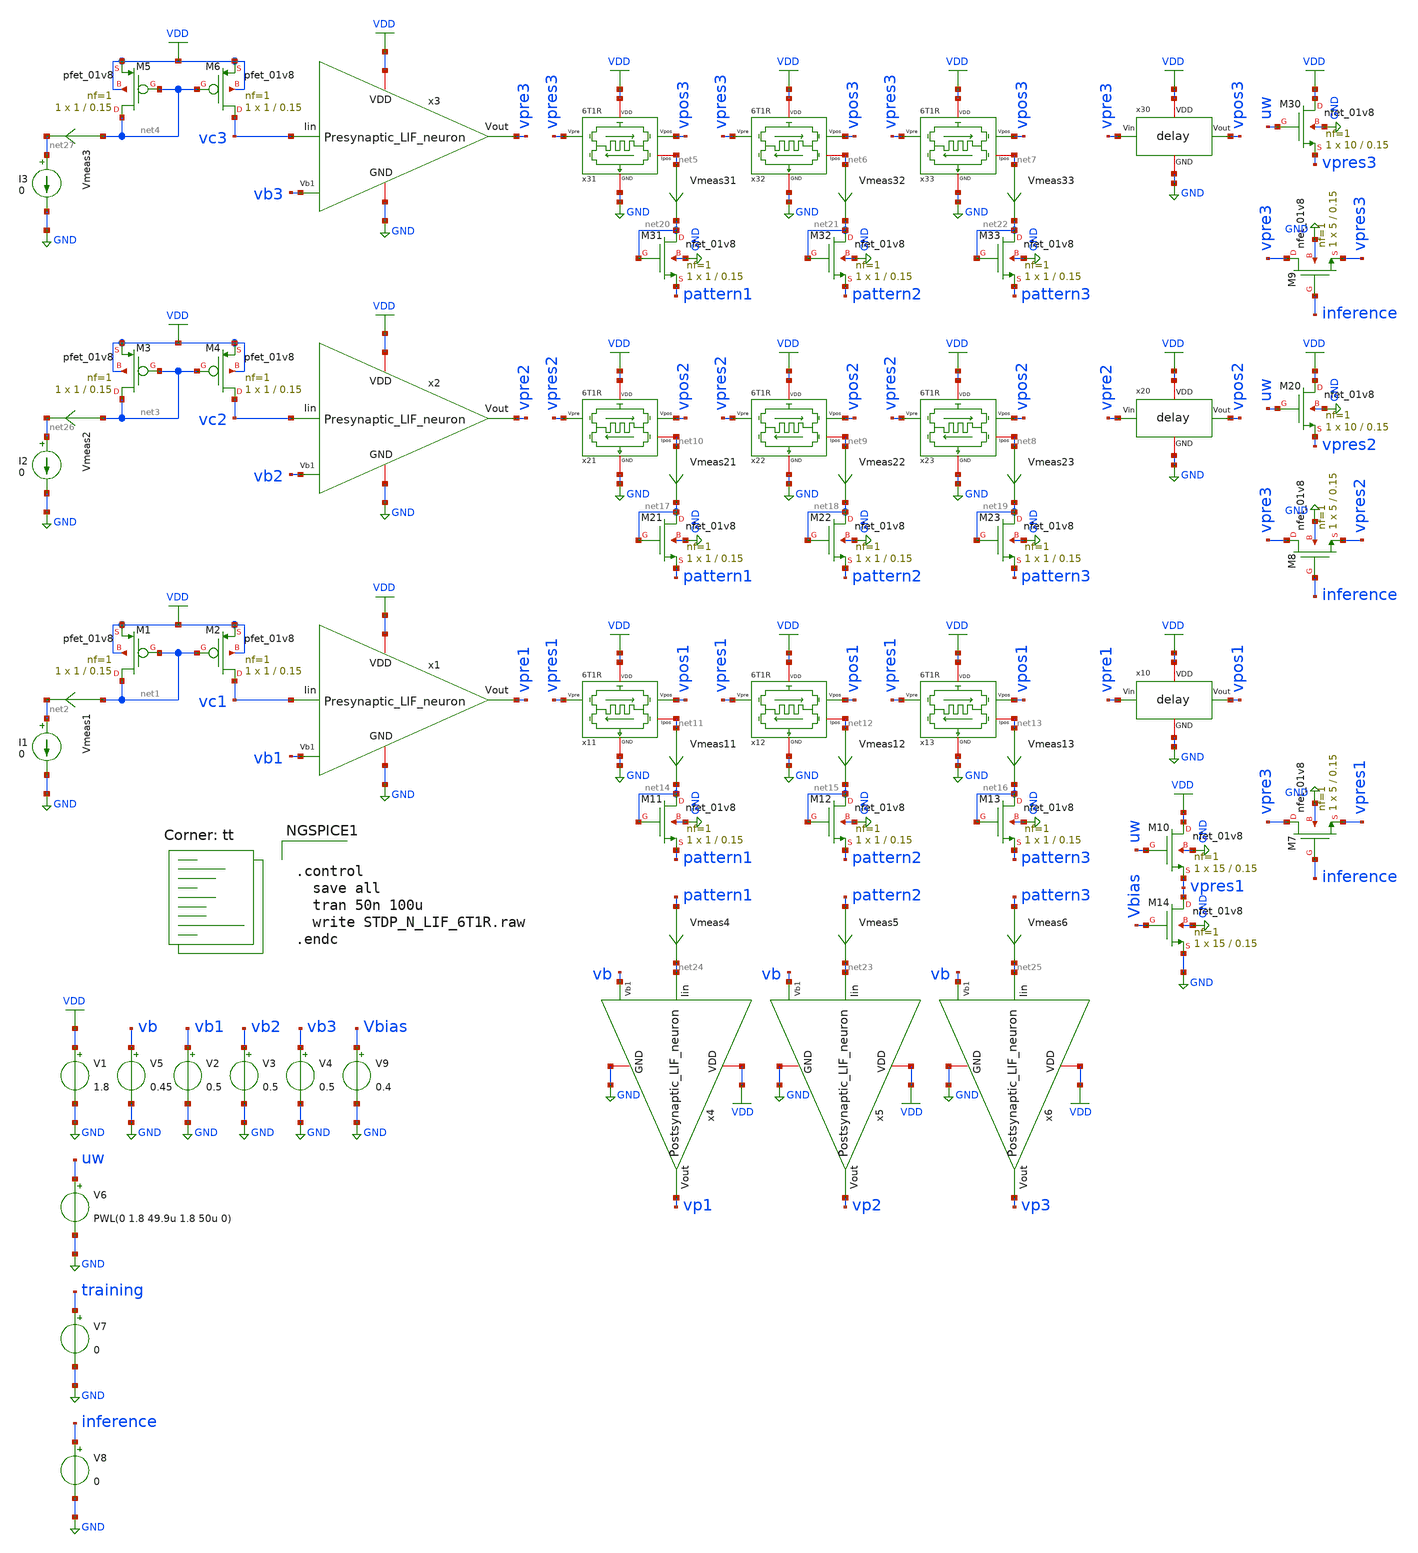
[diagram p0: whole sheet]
** sch_path: STDP/SNN_test.sch
**.subckt SNN_test
V1 VDD GND 1.8
V2 vb1 GND 0.5
I1 net2 GND 0
XM2 vc1 net1 VDD VDD sky130_fd_pr__pfet_01v8 L=0.15 W=1 nf=1 ad='int((nf+1)/2) * W/nf * 0.29' as='int((nf+2)/2) * W/nf * 0.29'
+ pd='2*int((nf+1)/2) * (W/nf + 0.29)' ps='2*int((nf+2)/2) * (W/nf + 0.29)' nrd='0.29 / W' nrs='0.29 / W'
+ sa=0 sb=0 sd=0 mult=1 m=1
XM1 net1 net1 VDD VDD sky130_fd_pr__pfet_01v8 L=0.15 W=1 nf=1 ad='int((nf+1)/2) * W/nf * 0.29' as='int((nf+2)/2) * W/nf * 0.29'
+ pd='2*int((nf+1)/2) * (W/nf + 0.29)' ps='2*int((nf+2)/2) * (W/nf + 0.29)' nrd='0.29 / W' nrs='0.29 / W'
+ sa=0 sb=0 sd=0 mult=1 m=1
Vmeas31 net5 net20 0
.save i(vmeas31)
V3 vb2 GND 0.5
V4 vb3 GND 0.5
x1 VDD vpre1 vb1 GND vc1 Presynaptic_LIF_neuron
x5 net23 VDD vp2 vb GND Postsynaptic_LIF_neuron
V5 vb GND 0.45
x2 VDD vpre2 vb2 GND vc2 Presynaptic_LIF_neuron
XM4 vc2 net3 VDD VDD sky130_fd_pr__pfet_01v8 L=0.15 W=1 nf=1 ad='int((nf+1)/2) * W/nf * 0.29' as='int((nf+2)/2) * W/nf * 0.29'
+ pd='2*int((nf+1)/2) * (W/nf + 0.29)' ps='2*int((nf+2)/2) * (W/nf + 0.29)' nrd='0.29 / W' nrs='0.29 / W'
+ sa=0 sb=0 sd=0 mult=1 m=1
XM3 net3 net3 VDD VDD sky130_fd_pr__pfet_01v8 L=0.15 W=1 nf=1 ad='int((nf+1)/2) * W/nf * 0.29' as='int((nf+2)/2) * W/nf * 0.29'
+ pd='2*int((nf+1)/2) * (W/nf + 0.29)' ps='2*int((nf+2)/2) * (W/nf + 0.29)' nrd='0.29 / W' nrs='0.29 / W'
+ sa=0 sb=0 sd=0 mult=1 m=1
x31 VDD net5 vpres3 vpos3 GND 6T1R
x3 VDD vpre3 vb3 GND vc3 Presynaptic_LIF_neuron
XM6 vc3 net4 VDD VDD sky130_fd_pr__pfet_01v8 L=0.15 W=1 nf=1 ad='int((nf+1)/2) * W/nf * 0.29' as='int((nf+2)/2) * W/nf * 0.29'
+ pd='2*int((nf+1)/2) * (W/nf + 0.29)' ps='2*int((nf+2)/2) * (W/nf + 0.29)' nrd='0.29 / W' nrs='0.29 / W'
+ sa=0 sb=0 sd=0 mult=1 m=1
XM5 net4 net4 VDD VDD sky130_fd_pr__pfet_01v8 L=0.15 W=1 nf=1 ad='int((nf+1)/2) * W/nf * 0.29' as='int((nf+2)/2) * W/nf * 0.29'
+ pd='2*int((nf+1)/2) * (W/nf + 0.29)' ps='2*int((nf+2)/2) * (W/nf + 0.29)' nrd='0.29 / W' nrs='0.29 / W'
+ sa=0 sb=0 sd=0 mult=1 m=1
x30 VDD vpre3 vpos3 GND delay
XM9 vpre3 inference vpres3 GND sky130_fd_pr__nfet_01v8 L=0.15 W=5 nf=1 ad='int((nf+1)/2) * W/nf * 0.29'
+ as='int((nf+2)/2) * W/nf * 0.29' pd='2*int((nf+1)/2) * (W/nf + 0.29)' ps='2*int((nf+2)/2) * (W/nf + 0.29)'
+ nrd='0.29 / W' nrs='0.29 / W' sa=0 sb=0 sd=0 mult=1 m=1
XM8 vpre3 inference vpres2 GND sky130_fd_pr__nfet_01v8 L=0.15 W=5 nf=1 ad='int((nf+1)/2) * W/nf * 0.29'
+ as='int((nf+2)/2) * W/nf * 0.29' pd='2*int((nf+1)/2) * (W/nf + 0.29)' ps='2*int((nf+2)/2) * (W/nf + 0.29)'
+ nrd='0.29 / W' nrs='0.29 / W' sa=0 sb=0 sd=0 mult=1 m=1
XM7 vpre3 inference vpres1 GND sky130_fd_pr__nfet_01v8 L=0.15 W=5 nf=1 ad='int((nf+1)/2) * W/nf * 0.29'
+ as='int((nf+2)/2) * W/nf * 0.29' pd='2*int((nf+1)/2) * (W/nf + 0.29)' ps='2*int((nf+2)/2) * (W/nf + 0.29)'
+ nrd='0.29 / W' nrs='0.29 / W' sa=0 sb=0 sd=0 mult=1 m=1
x11 VDD net11 vpres1 vpos1 GND 6T1R
x10 VDD vpre1 vpos1 GND delay
x21 VDD net10 vpres2 vpos2 GND 6T1R
x20 VDD vpre2 vpos2 GND delay
x32 VDD net6 vpres3 vpos3 GND 6T1R
x12 VDD net12 vpres1 vpos1 GND 6T1R
x22 VDD net9 vpres2 vpos2 GND 6T1R
x33 VDD net7 vpres3 vpos3 GND 6T1R
x13 VDD net13 vpres1 vpos1 GND 6T1R
x23 VDD net8 vpres2 vpos2 GND 6T1R
Vmeas32 net6 net21 0
.save i(vmeas32)
Vmeas33 net7 net22 0
.save i(vmeas33)
Vmeas23 net8 net19 0
.save i(vmeas23)
Vmeas22 net9 net18 0
.save i(vmeas22)
Vmeas21 net10 net17 0
.save i(vmeas21)
Vmeas11 net11 net14 0
.save i(vmeas11)
Vmeas12 net12 net15 0
.save i(vmeas12)
Vmeas13 net13 net16 0
.save i(vmeas13)
XM11 net14 net14 pattern1 GND sky130_fd_pr__nfet_01v8 L=0.15 W=1 nf=1 ad='int((nf+1)/2) * W/nf * 0.29'
+ as='int((nf+2)/2) * W/nf * 0.29' pd='2*int((nf+1)/2) * (W/nf + 0.29)' ps='2*int((nf+2)/2) * (W/nf + 0.29)'
+ nrd='0.29 / W' nrs='0.29 / W' sa=0 sb=0 sd=0 mult=1 m=1
XM12 net15 net15 pattern2 GND sky130_fd_pr__nfet_01v8 L=0.15 W=1 nf=1 ad='int((nf+1)/2) * W/nf * 0.29'
+ as='int((nf+2)/2) * W/nf * 0.29' pd='2*int((nf+1)/2) * (W/nf + 0.29)' ps='2*int((nf+2)/2) * (W/nf + 0.29)'
+ nrd='0.29 / W' nrs='0.29 / W' sa=0 sb=0 sd=0 mult=1 m=1
XM13 net16 net16 pattern3 GND sky130_fd_pr__nfet_01v8 L=0.15 W=1 nf=1 ad='int((nf+1)/2) * W/nf * 0.29'
+ as='int((nf+2)/2) * W/nf * 0.29' pd='2*int((nf+1)/2) * (W/nf + 0.29)' ps='2*int((nf+2)/2) * (W/nf + 0.29)'
+ nrd='0.29 / W' nrs='0.29 / W' sa=0 sb=0 sd=0 mult=1 m=1
XM21 net17 net17 pattern1 GND sky130_fd_pr__nfet_01v8 L=0.15 W=1 nf=1 ad='int((nf+1)/2) * W/nf * 0.29'
+ as='int((nf+2)/2) * W/nf * 0.29' pd='2*int((nf+1)/2) * (W/nf + 0.29)' ps='2*int((nf+2)/2) * (W/nf + 0.29)'
+ nrd='0.29 / W' nrs='0.29 / W' sa=0 sb=0 sd=0 mult=1 m=1
XM22 net18 net18 pattern2 GND sky130_fd_pr__nfet_01v8 L=0.15 W=1 nf=1 ad='int((nf+1)/2) * W/nf * 0.29'
+ as='int((nf+2)/2) * W/nf * 0.29' pd='2*int((nf+1)/2) * (W/nf + 0.29)' ps='2*int((nf+2)/2) * (W/nf + 0.29)'
+ nrd='0.29 / W' nrs='0.29 / W' sa=0 sb=0 sd=0 mult=1 m=1
XM23 net19 net19 pattern3 GND sky130_fd_pr__nfet_01v8 L=0.15 W=1 nf=1 ad='int((nf+1)/2) * W/nf * 0.29'
+ as='int((nf+2)/2) * W/nf * 0.29' pd='2*int((nf+1)/2) * (W/nf + 0.29)' ps='2*int((nf+2)/2) * (W/nf + 0.29)'
+ nrd='0.29 / W' nrs='0.29 / W' sa=0 sb=0 sd=0 mult=1 m=1
XM31 net20 net20 pattern1 GND sky130_fd_pr__nfet_01v8 L=0.15 W=1 nf=1 ad='int((nf+1)/2) * W/nf * 0.29'
+ as='int((nf+2)/2) * W/nf * 0.29' pd='2*int((nf+1)/2) * (W/nf + 0.29)' ps='2*int((nf+2)/2) * (W/nf + 0.29)'
+ nrd='0.29 / W' nrs='0.29 / W' sa=0 sb=0 sd=0 mult=1 m=1
XM32 net21 net21 pattern2 GND sky130_fd_pr__nfet_01v8 L=0.15 W=1 nf=1 ad='int((nf+1)/2) * W/nf * 0.29'
+ as='int((nf+2)/2) * W/nf * 0.29' pd='2*int((nf+1)/2) * (W/nf + 0.29)' ps='2*int((nf+2)/2) * (W/nf + 0.29)'
+ nrd='0.29 / W' nrs='0.29 / W' sa=0 sb=0 sd=0 mult=1 m=1
XM33 net22 net22 pattern3 GND sky130_fd_pr__nfet_01v8 L=0.15 W=1 nf=1 ad='int((nf+1)/2) * W/nf * 0.29'
+ as='int((nf+2)/2) * W/nf * 0.29' pd='2*int((nf+1)/2) * (W/nf + 0.29)' ps='2*int((nf+2)/2) * (W/nf + 0.29)'
+ nrd='0.29 / W' nrs='0.29 / W' sa=0 sb=0 sd=0 mult=1 m=1
XM10 VDD uw vpres1 GND sky130_fd_pr__nfet_01v8 L=0.15 W=15 nf=1 ad='int((nf+1)/2) * W/nf * 0.29' as='int((nf+2)/2) * W/nf * 0.29'
+ pd='2*int((nf+1)/2) * (W/nf + 0.29)' ps='2*int((nf+2)/2) * (W/nf + 0.29)' nrd='0.29 / W' nrs='0.29 / W'
+ sa=0 sb=0 sd=0 mult=1 m=1
XM20 VDD uw vpres2 GND sky130_fd_pr__nfet_01v8 L=0.15 W=10 nf=1 ad='int((nf+1)/2) * W/nf * 0.29' as='int((nf+2)/2) * W/nf * 0.29'
+ pd='2*int((nf+1)/2) * (W/nf + 0.29)' ps='2*int((nf+2)/2) * (W/nf + 0.29)' nrd='0.29 / W' nrs='0.29 / W'
+ sa=0 sb=0 sd=0 mult=1 m=1
XM30 VDD uw vpres3 GND sky130_fd_pr__nfet_01v8 L=0.15 W=10 nf=1 ad='int((nf+1)/2) * W/nf * 0.29' as='int((nf+2)/2) * W/nf * 0.29'
+ pd='2*int((nf+1)/2) * (W/nf + 0.29)' ps='2*int((nf+2)/2) * (W/nf + 0.29)' nrd='0.29 / W' nrs='0.29 / W'
+ sa=0 sb=0 sd=0 mult=1 m=1
Vmeas5 pattern2 net23 0
.save i(vmeas5)
x4 net24 VDD vp1 vb GND Postsynaptic_LIF_neuron
Vmeas4 pattern1 net24 0
.save i(vmeas4)
x6 net25 VDD vp3 vb GND Postsynaptic_LIF_neuron
Vmeas6 pattern3 net25 0
.save i(vmeas6)
V6 uw GND PWL(0 1.8 49.9u 1.8 50u 0)
V7 training GND 0
V8 inference GND 0
Vmeas1 net1 net2 0
.save i(vmeas1)
I2 net26 GND 0
Vmeas2 net3 net26 0
.save i(vmeas2)
I3 net27 GND 0
Vmeas3 net4 net27 0
.save i(vmeas3)
XM14 vpres1 Vbias GND GND sky130_fd_pr__nfet_01v8 L=0.15 W=15 nf=1 ad='int((nf+1)/2) * W/nf * 0.29' as='int((nf+2)/2) * W/nf * 0.29'
+ pd='2*int((nf+1)/2) * (W/nf + 0.29)' ps='2*int((nf+2)/2) * (W/nf + 0.29)' nrd='0.29 / W' nrs='0.29 / W'
+ sa=0 sb=0 sd=0 mult=1 m=1
V9 Vbias GND 0.4
**** begin user architecture code
.lib $::SKYWATER_MODELS/sky130.lib.spice tt

** opencircuitdesign pdks install
.inc $::SKYWATER_MODELS/rram_v0.spice



.control
  save all
  tran 50n 100u
  write STDP_N_LIF_6T1R.raw
.endc


**** end user architecture code
**.ends

* expanding   symbol:
*+  /home/ricardo/RATT_repos/Proyectos_xschem/LIF_neuron/Presynaptic_LIF_neuron.sym # of pins=5
** sym_path: LIF_neuron/Presynaptic_LIF_neuron.sym
** sch_path: LIF_neuron/Presynaptic_LIF_neuron.sch
.subckt Presynaptic_LIF_neuron VDD Vout Vb1 GND Iin
*.iopin GND
*.ipin Vb1
*.iopin VDD
*.opin Vout
*.ipin Iin
XM13 net2 Vb1 GND GND sky130_fd_pr__nfet_01v8 L=0.5 W=5 nf=1 ad='int((nf+1)/2) * W/nf * 0.29' as='int((nf+2)/2) * W/nf * 0.29'
+ pd='2*int((nf+1)/2) * (W/nf + 0.29)' ps='2*int((nf+2)/2) * (W/nf + 0.29)' nrd='0.29 / W' nrs='0.29 / W'
+ sa=0 sb=0 sd=0 mult=1 m=1
XM12 Crefr net1 net2 GND sky130_fd_pr__nfet_01v8 L=1 W=1 nf=1 ad='int((nf+1)/2) * W/nf * 0.29' as='int((nf+2)/2) * W/nf * 0.29'
+ pd='2*int((nf+1)/2) * (W/nf + 0.29)' ps='2*int((nf+2)/2) * (W/nf + 0.29)' nrd='0.29 / W' nrs='0.29 / W'
+ sa=0 sb=0 sd=0 mult=1 m=1
XM11 Crefr net1 VDD VDD sky130_fd_pr__pfet_01v8 L=1 W=1 nf=1 ad='int((nf+1)/2) * W/nf * 0.29' as='int((nf+2)/2) * W/nf * 0.29'
+ pd='2*int((nf+1)/2) * (W/nf + 0.29)' ps='2*int((nf+2)/2) * (W/nf + 0.29)' nrd='0.29 / W' nrs='0.29 / W'
+ sa=0 sb=0 sd=0 mult=1 m=1
XCrefr Crefr GND sky130_fd_pr__cap_mim_m3_1 W=10 L=1 MF=1 m=1
XM14 Iin Crefr GND GND sky130_fd_pr__nfet_01v8 L=6 W=0.45 nf=1 ad='int((nf+1)/2) * W/nf * 0.29' as='int((nf+2)/2) * W/nf * 0.29'
+ pd='2*int((nf+1)/2) * (W/nf + 0.29)' ps='2*int((nf+2)/2) * (W/nf + 0.29)' nrd='0.29 / W' nrs='0.29 / W'
+ sa=0 sb=0 sd=0 mult=1 m=1
XCm Iin GND sky130_fd_pr__cap_mim_m3_1 W=10 L=1 MF=30 m=30
XM6 net3 Vout GND GND sky130_fd_pr__nfet_01v8 L=0.5 W=1 nf=1 ad='int((nf+1)/2) * W/nf * 0.29' as='int((nf+2)/2) * W/nf * 0.29'
+ pd='2*int((nf+1)/2) * (W/nf + 0.29)' ps='2*int((nf+2)/2) * (W/nf + 0.29)' nrd='0.29 / W' nrs='0.29 / W'
+ sa=0 sb=0 sd=0 mult=1 m=1
XM7 net1 Iin net3 GND sky130_fd_pr__nfet_01v8 L=1 W=1 nf=1 ad='int((nf+1)/2) * W/nf * 0.29' as='int((nf+2)/2) * W/nf * 0.29'
+ pd='2*int((nf+1)/2) * (W/nf + 0.29)' ps='2*int((nf+2)/2) * (W/nf + 0.29)' nrd='0.29 / W' nrs='0.29 / W'
+ sa=0 sb=0 sd=0 mult=1 m=1
XM8 net1 Iin VDD VDD sky130_fd_pr__pfet_01v8 L=1 W=1 nf=1 ad='int((nf+1)/2) * W/nf * 0.29' as='int((nf+2)/2) * W/nf * 0.29'
+ pd='2*int((nf+1)/2) * (W/nf + 0.29)' ps='2*int((nf+2)/2) * (W/nf + 0.29)' nrd='0.29 / W' nrs='0.29 / W'
+ sa=0 sb=0 sd=0 mult=1 m=1
XM9 Vout net1 net3 GND sky130_fd_pr__nfet_01v8 L=1 W=1 nf=1 ad='int((nf+1)/2) * W/nf * 0.29' as='int((nf+2)/2) * W/nf * 0.29'
+ pd='2*int((nf+1)/2) * (W/nf + 0.29)' ps='2*int((nf+2)/2) * (W/nf + 0.29)' nrd='0.29 / W' nrs='0.29 / W'
+ sa=0 sb=0 sd=0 mult=1 m=1
XM10 Vout net1 VDD VDD sky130_fd_pr__pfet_01v8 L=1 W=5 nf=1 ad='int((nf+1)/2) * W/nf * 0.29' as='int((nf+2)/2) * W/nf * 0.29'
+ pd='2*int((nf+1)/2) * (W/nf + 0.29)' ps='2*int((nf+2)/2) * (W/nf + 0.29)' nrd='0.29 / W' nrs='0.29 / W'
+ sa=0 sb=0 sd=0 mult=1 m=1
.ends


* expanding   symbol:
*+  /home/ricardo/RATT_repos/Proyectos_xschem/LIF_neuron/Postsynaptic_LIF_neuron.sym # of pins=5
** sym_path: LIF_neuron/Postsynaptic_LIF_neuron.sym
** sch_path: LIF_neuron/Postsynaptic_LIF_neuron.sch
.subckt Postsynaptic_LIF_neuron Iin VDD Vout Vb1 GND
*.iopin GND
*.ipin Vb1
*.iopin VDD
*.opin Vout
*.ipin Iin
XM13 net2 Vb1 GND GND sky130_fd_pr__nfet_01v8 L=0.5 W=5 nf=1 ad='int((nf+1)/2) * W/nf * 0.29' as='int((nf+2)/2) * W/nf * 0.29'
+ pd='2*int((nf+1)/2) * (W/nf + 0.29)' ps='2*int((nf+2)/2) * (W/nf + 0.29)' nrd='0.29 / W' nrs='0.29 / W'
+ sa=0 sb=0 sd=0 mult=1 m=1
XM12 Crefr net1 net2 GND sky130_fd_pr__nfet_01v8 L=1 W=1 nf=1 ad='int((nf+1)/2) * W/nf * 0.29' as='int((nf+2)/2) * W/nf * 0.29'
+ pd='2*int((nf+1)/2) * (W/nf + 0.29)' ps='2*int((nf+2)/2) * (W/nf + 0.29)' nrd='0.29 / W' nrs='0.29 / W'
+ sa=0 sb=0 sd=0 mult=1 m=1
XM11 Crefr net1 VDD VDD sky130_fd_pr__pfet_01v8 L=1 W=1 nf=1 ad='int((nf+1)/2) * W/nf * 0.29' as='int((nf+2)/2) * W/nf * 0.29'
+ pd='2*int((nf+1)/2) * (W/nf + 0.29)' ps='2*int((nf+2)/2) * (W/nf + 0.29)' nrd='0.29 / W' nrs='0.29 / W'
+ sa=0 sb=0 sd=0 mult=1 m=1
XC1 Crefr GND sky130_fd_pr__cap_mim_m3_1 W=21 L=1 MF=1 m=1
XM14 Iin Crefr GND GND sky130_fd_pr__nfet_01v8 L=40 W=1 nf=1 ad='int((nf+1)/2) * W/nf * 0.29' as='int((nf+2)/2) * W/nf * 0.29'
+ pd='2*int((nf+1)/2) * (W/nf + 0.29)' ps='2*int((nf+2)/2) * (W/nf + 0.29)' nrd='0.29 / W' nrs='0.29 / W'
+ sa=0 sb=0 sd=0 mult=1 m=1
XC2 Iin GND sky130_fd_pr__cap_mim_m3_1 W=20 L=1 MF=50 m=50
XM6 net3 Vout GND GND sky130_fd_pr__nfet_01v8 L=0.5 W=1 nf=1 ad='int((nf+1)/2) * W/nf * 0.29' as='int((nf+2)/2) * W/nf * 0.29'
+ pd='2*int((nf+1)/2) * (W/nf + 0.29)' ps='2*int((nf+2)/2) * (W/nf + 0.29)' nrd='0.29 / W' nrs='0.29 / W'
+ sa=0 sb=0 sd=0 mult=1 m=1
XM7 net1 Iin net3 GND sky130_fd_pr__nfet_01v8 L=1 W=1 nf=1 ad='int((nf+1)/2) * W/nf * 0.29' as='int((nf+2)/2) * W/nf * 0.29'
+ pd='2*int((nf+1)/2) * (W/nf + 0.29)' ps='2*int((nf+2)/2) * (W/nf + 0.29)' nrd='0.29 / W' nrs='0.29 / W'
+ sa=0 sb=0 sd=0 mult=1 m=1
XM8 net1 Iin VDD VDD sky130_fd_pr__pfet_01v8 L=1 W=1 nf=1 ad='int((nf+1)/2) * W/nf * 0.29' as='int((nf+2)/2) * W/nf * 0.29'
+ pd='2*int((nf+1)/2) * (W/nf + 0.29)' ps='2*int((nf+2)/2) * (W/nf + 0.29)' nrd='0.29 / W' nrs='0.29 / W'
+ sa=0 sb=0 sd=0 mult=1 m=1
XM9 Vout net1 net3 GND sky130_fd_pr__nfet_01v8 L=1 W=1 nf=1 ad='int((nf+1)/2) * W/nf * 0.29' as='int((nf+2)/2) * W/nf * 0.29'
+ pd='2*int((nf+1)/2) * (W/nf + 0.29)' ps='2*int((nf+2)/2) * (W/nf + 0.29)' nrd='0.29 / W' nrs='0.29 / W'
+ sa=0 sb=0 sd=0 mult=1 m=1
XM10 Vout net1 VDD VDD sky130_fd_pr__pfet_01v8 L=1 W=5 nf=1 ad='int((nf+1)/2) * W/nf * 0.29' as='int((nf+2)/2) * W/nf * 0.29'
+ pd='2*int((nf+1)/2) * (W/nf + 0.29)' ps='2*int((nf+2)/2) * (W/nf + 0.29)' nrd='0.29 / W' nrs='0.29 / W'
+ sa=0 sb=0 sd=0 mult=1 m=1
.ends


* expanding   symbol:  /home/ricardo/RATT_repos/Proyectos_xschem/synapse/6T1R.sym # of pins=5
** sym_path: synapse/6T1R.sym
** sch_path: synapse/6T1R.sch
.subckt 6T1R VDD Ipos Vpre Vpos GND
*.ipin Vpre
*.ipin Vpos
*.iopin GND
*.iopin Ipos
*.iopin VDD
XM1 vipre Vpre BE GND sky130_fd_pr__nfet_01v8 L=0.15 W=10 nf=1 ad='int((nf+1)/2) * W/nf * 0.29' as='int((nf+2)/2) * W/nf * 0.29'
+ pd='2*int((nf+1)/2) * (W/nf + 0.29)' ps='2*int((nf+2)/2) * (W/nf + 0.29)' nrd='0.29 / W' nrs='0.29 / W'
+ sa=0 sb=0 sd=0 mult=1 m=1
XR1 TE BE rram_v0
XM3 vipre Vpos TE GND sky130_fd_pr__nfet_01v8 L=0.15 W=20 nf=1 ad='int((nf+1)/2) * W/nf * 0.29' as='int((nf+2)/2) * W/nf * 0.29'
+ pd='2*int((nf+1)/2) * (W/nf + 0.29)' ps='2*int((nf+2)/2) * (W/nf + 0.29)' nrd='0.29 / W' nrs='0.29 / W'
+ sa=0 sb=0 sd=0 mult=1 m=1
XM6 Ipos vipre VDD VDD sky130_fd_pr__pfet_01v8 L=0.15 W=20 nf=1 ad='int((nf+1)/2) * W/nf * 0.29' as='int((nf+2)/2) * W/nf * 0.29'
+ pd='2*int((nf+1)/2) * (W/nf + 0.29)' ps='2*int((nf+2)/2) * (W/nf + 0.29)' nrd='0.29 / W' nrs='0.29 / W'
+ sa=0 sb=0 sd=0 mult=1 m=1
XM5 vipre vipre VDD VDD sky130_fd_pr__pfet_01v8 L=0.15 W=20 nf=1 ad='int((nf+1)/2) * W/nf * 0.29' as='int((nf+2)/2) * W/nf * 0.29'
+ pd='2*int((nf+1)/2) * (W/nf + 0.29)' ps='2*int((nf+2)/2) * (W/nf + 0.29)' nrd='0.29 / W' nrs='0.29 / W'
+ sa=0 sb=0 sd=0 mult=1 m=1
XM2 BE Vpos GND GND sky130_fd_pr__nfet_01v8 L=0.15 W=20 nf=1 ad='int((nf+1)/2) * W/nf * 0.29' as='int((nf+2)/2) * W/nf * 0.29'
+ pd='2*int((nf+1)/2) * (W/nf + 0.29)' ps='2*int((nf+2)/2) * (W/nf + 0.29)' nrd='0.29 / W' nrs='0.29 / W'
+ sa=0 sb=0 sd=0 mult=1 m=1
XM4 TE Vpre GND GND sky130_fd_pr__nfet_01v8 L=0.15 W=10 nf=1 ad='int((nf+1)/2) * W/nf * 0.29' as='int((nf+2)/2) * W/nf * 0.29'
+ pd='2*int((nf+1)/2) * (W/nf + 0.29)' ps='2*int((nf+2)/2) * (W/nf + 0.29)' nrd='0.29 / W' nrs='0.29 / W'
+ sa=0 sb=0 sd=0 mult=1 m=1
.ends


* expanding   symbol:  /home/ricardo/RATT_repos/Proyectos_xschem/delay/delay.sym # of pins=4
** sym_path: delay/delay.sym
** sch_path: delay/delay.sch
.subckt delay VDD Vin Vout GND
*.ipin Vin
*.opin Vout
*.iopin VDD
*.iopin GND
XM1 net1 Vin VDD VDD sky130_fd_pr__pfet_01v8 L=6 W=0.45 nf=1 ad='int((nf+1)/2) * W/nf * 0.29' as='int((nf+2)/2) * W/nf * 0.29'
+ pd='2*int((nf+1)/2) * (W/nf + 0.29)' ps='2*int((nf+2)/2) * (W/nf + 0.29)' nrd='0.29 / W' nrs='0.29 / W'
+ sa=0 sb=0 sd=0 mult=1 m=1
XM2 net1 Vin GND GND sky130_fd_pr__nfet_01v8 L=6 W=0.45 nf=1 ad='int((nf+1)/2) * W/nf * 0.29' as='int((nf+2)/2) * W/nf * 0.29'
+ pd='2*int((nf+1)/2) * (W/nf + 0.29)' ps='2*int((nf+2)/2) * (W/nf + 0.29)' nrd='0.29 / W' nrs='0.29 / W'
+ sa=0 sb=0 sd=0 mult=1 m=1
XM3 net2 net1 VDD VDD sky130_fd_pr__pfet_01v8 L=6 W=0.45 nf=1 ad='int((nf+1)/2) * W/nf * 0.29' as='int((nf+2)/2) * W/nf * 0.29'
+ pd='2*int((nf+1)/2) * (W/nf + 0.29)' ps='2*int((nf+2)/2) * (W/nf + 0.29)' nrd='0.29 / W' nrs='0.29 / W'
+ sa=0 sb=0 sd=0 mult=1 m=1
XM4 net2 net1 GND GND sky130_fd_pr__nfet_01v8 L=6 W=0.45 nf=1 ad='int((nf+1)/2) * W/nf * 0.29' as='int((nf+2)/2) * W/nf * 0.29'
+ pd='2*int((nf+1)/2) * (W/nf + 0.29)' ps='2*int((nf+2)/2) * (W/nf + 0.29)' nrd='0.29 / W' nrs='0.29 / W'
+ sa=0 sb=0 sd=0 mult=1 m=1
XM5 net3 net2 VDD VDD sky130_fd_pr__pfet_01v8 L=6 W=0.45 nf=1 ad='int((nf+1)/2) * W/nf * 0.29' as='int((nf+2)/2) * W/nf * 0.29'
+ pd='2*int((nf+1)/2) * (W/nf + 0.29)' ps='2*int((nf+2)/2) * (W/nf + 0.29)' nrd='0.29 / W' nrs='0.29 / W'
+ sa=0 sb=0 sd=0 mult=1 m=1
XM6 net3 net2 GND GND sky130_fd_pr__nfet_01v8 L=6 W=0.45 nf=1 ad='int((nf+1)/2) * W/nf * 0.29' as='int((nf+2)/2) * W/nf * 0.29'
+ pd='2*int((nf+1)/2) * (W/nf + 0.29)' ps='2*int((nf+2)/2) * (W/nf + 0.29)' nrd='0.29 / W' nrs='0.29 / W'
+ sa=0 sb=0 sd=0 mult=1 m=1
XM7 Vout net3 VDD VDD sky130_fd_pr__pfet_01v8 L=6 W=0.45 nf=1 ad='int((nf+1)/2) * W/nf * 0.29' as='int((nf+2)/2) * W/nf * 0.29'
+ pd='2*int((nf+1)/2) * (W/nf + 0.29)' ps='2*int((nf+2)/2) * (W/nf + 0.29)' nrd='0.29 / W' nrs='0.29 / W'
+ sa=0 sb=0 sd=0 mult=1 m=1
XM8 Vout net3 GND GND sky130_fd_pr__nfet_01v8 L=6 W=0.45 nf=1 ad='int((nf+1)/2) * W/nf * 0.29' as='int((nf+2)/2) * W/nf * 0.29'
+ pd='2*int((nf+1)/2) * (W/nf + 0.29)' ps='2*int((nf+2)/2) * (W/nf + 0.29)' nrd='0.29 / W' nrs='0.29 / W'
+ sa=0 sb=0 sd=0 mult=1 m=1
.ends

.GLOBAL GND
.GLOBAL VDD
.end
